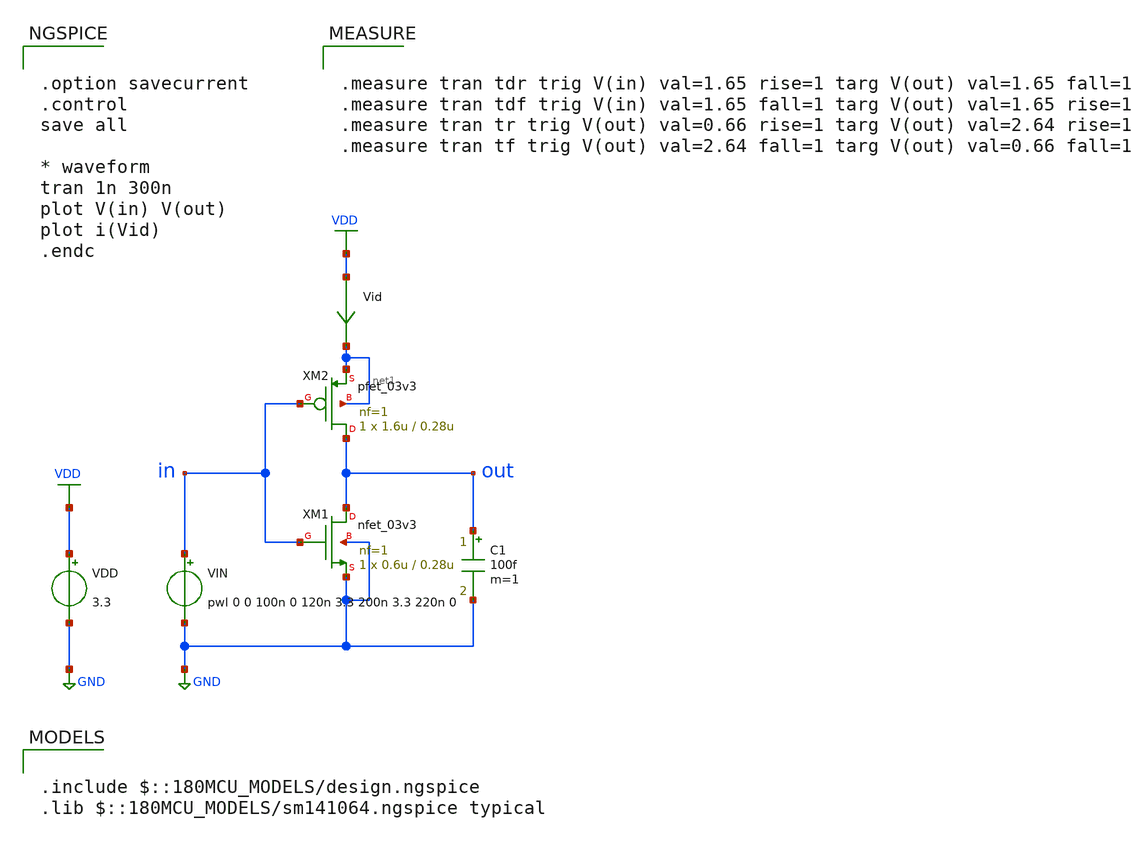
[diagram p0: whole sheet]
** sch_path: fifty_nifty/01_inv_tran.sch
**.subckt 01_inv_tran
XM1 out in GND GND nfet_03v3 L=0.28u W=0.6u nf=1 ad='int((nf+1)/2) * W/nf * 0.18u' as='int((nf+2)/2) * W/nf * 0.18u'
+ pd='2*int((nf+1)/2) * (W/nf + 0.18u)' ps='2*int((nf+2)/2) * (W/nf + 0.18u)' nrd='0.18u / W' nrs='0.18u / W'
+ sa=0 sb=0 sd=0 m=1
VIN in GND pwl 0 0 100n 0 120n 3.3 200n 3.3 220n 0
Vid VDD net1 0
.save i(vid)
XM2 out in net1 net1 pfet_03v3 L=0.28u W=1.6u nf=1 ad='int((nf+1)/2) * W/nf * 0.18u' as='int((nf+2)/2) * W/nf * 0.18u'
+ pd='2*int((nf+1)/2) * (W/nf + 0.18u)' ps='2*int((nf+2)/2) * (W/nf + 0.18u)' nrd='0.18u / W' nrs='0.18u / W'
+ sa=0 sb=0 sd=0 m=1
VDD VDD GND 3.3
C1 out GND 100f m=1
**** begin user architecture code

.option savecurrent
.control
save all

* waveform
tran 1n 300n
plot V(in) V(out)
plot i(Vid)
.endc


.include $::180MCU_MODELS/design.ngspice
.lib $::180MCU_MODELS/sm141064.ngspice typical


.measure tran tdr trig V(in) val=1.65 rise=1 targ V(out) val=1.65 fall=1
.measure tran tdf trig V(in) val=1.65 fall=1 targ V(out) val=1.65 rise=1
.measure tran tr trig V(out) val=0.66 rise=1 targ V(out) val=2.64 rise=1
.measure tran tf trig V(out) val=2.64 fall=1 targ V(out) val=0.66 fall=1

**** end user architecture code
**.ends
.GLOBAL GND
.GLOBAL VDD
.end
